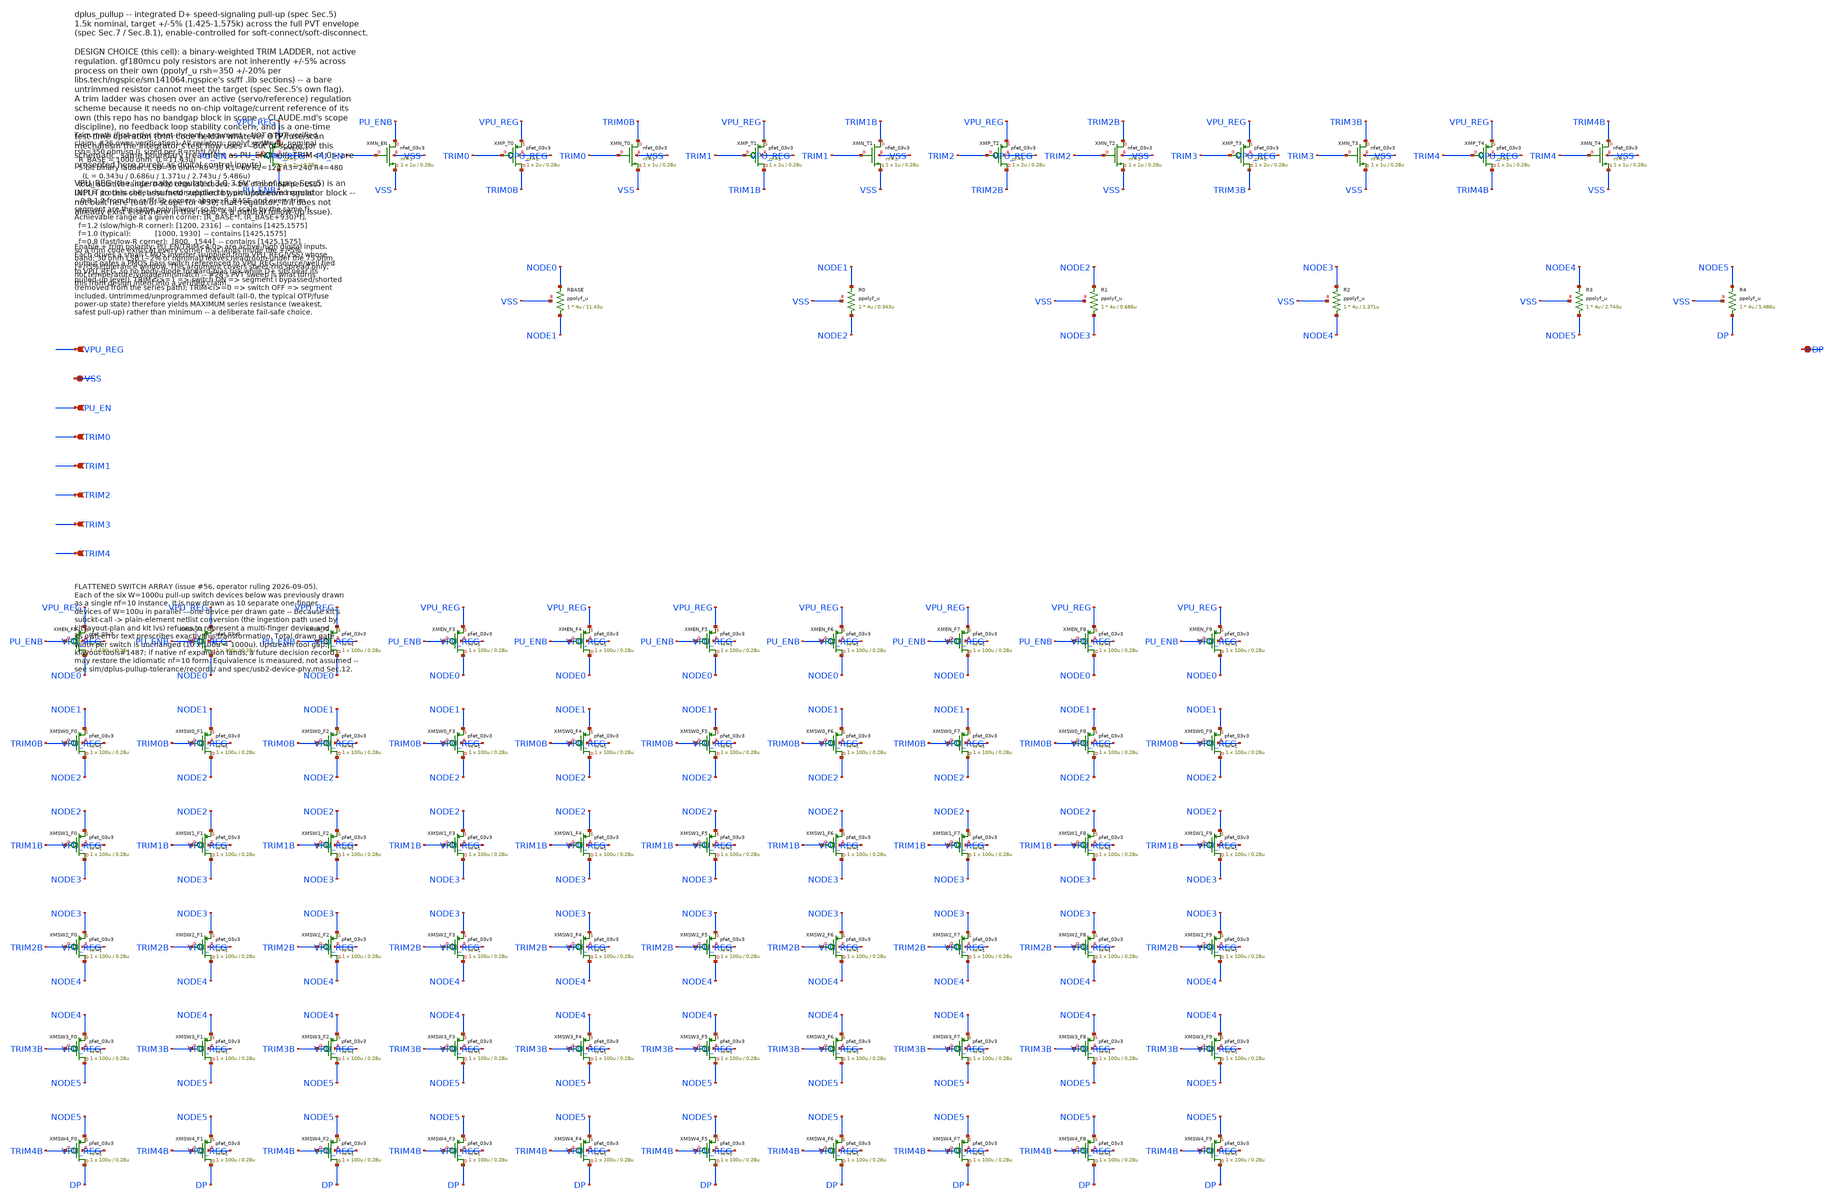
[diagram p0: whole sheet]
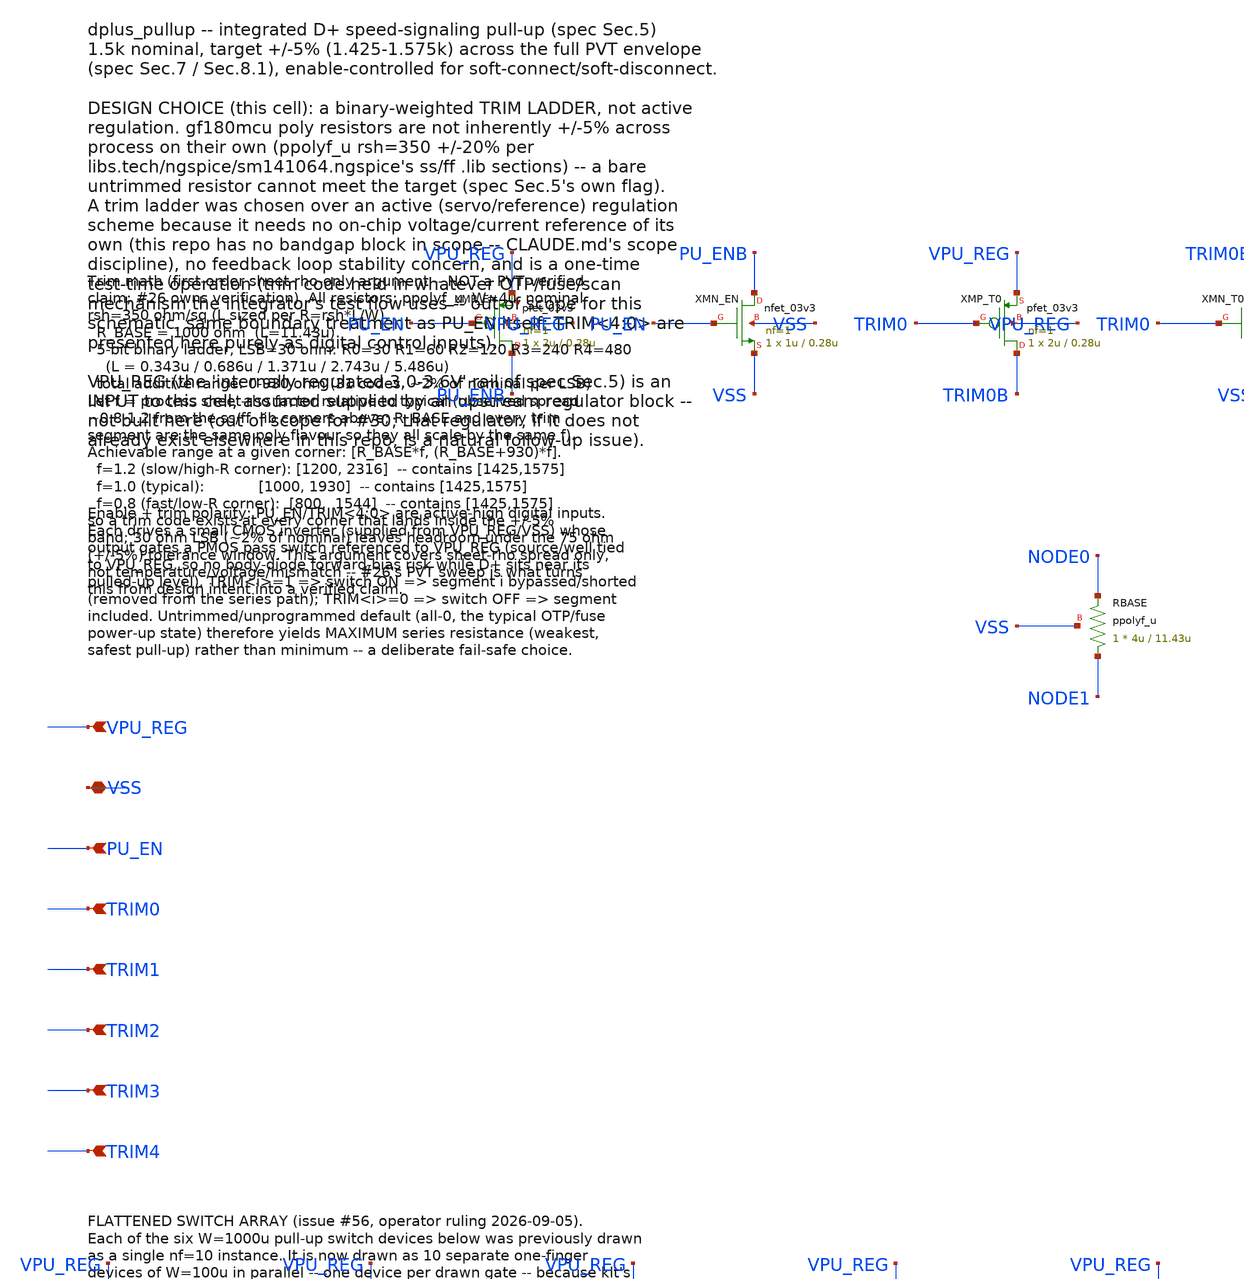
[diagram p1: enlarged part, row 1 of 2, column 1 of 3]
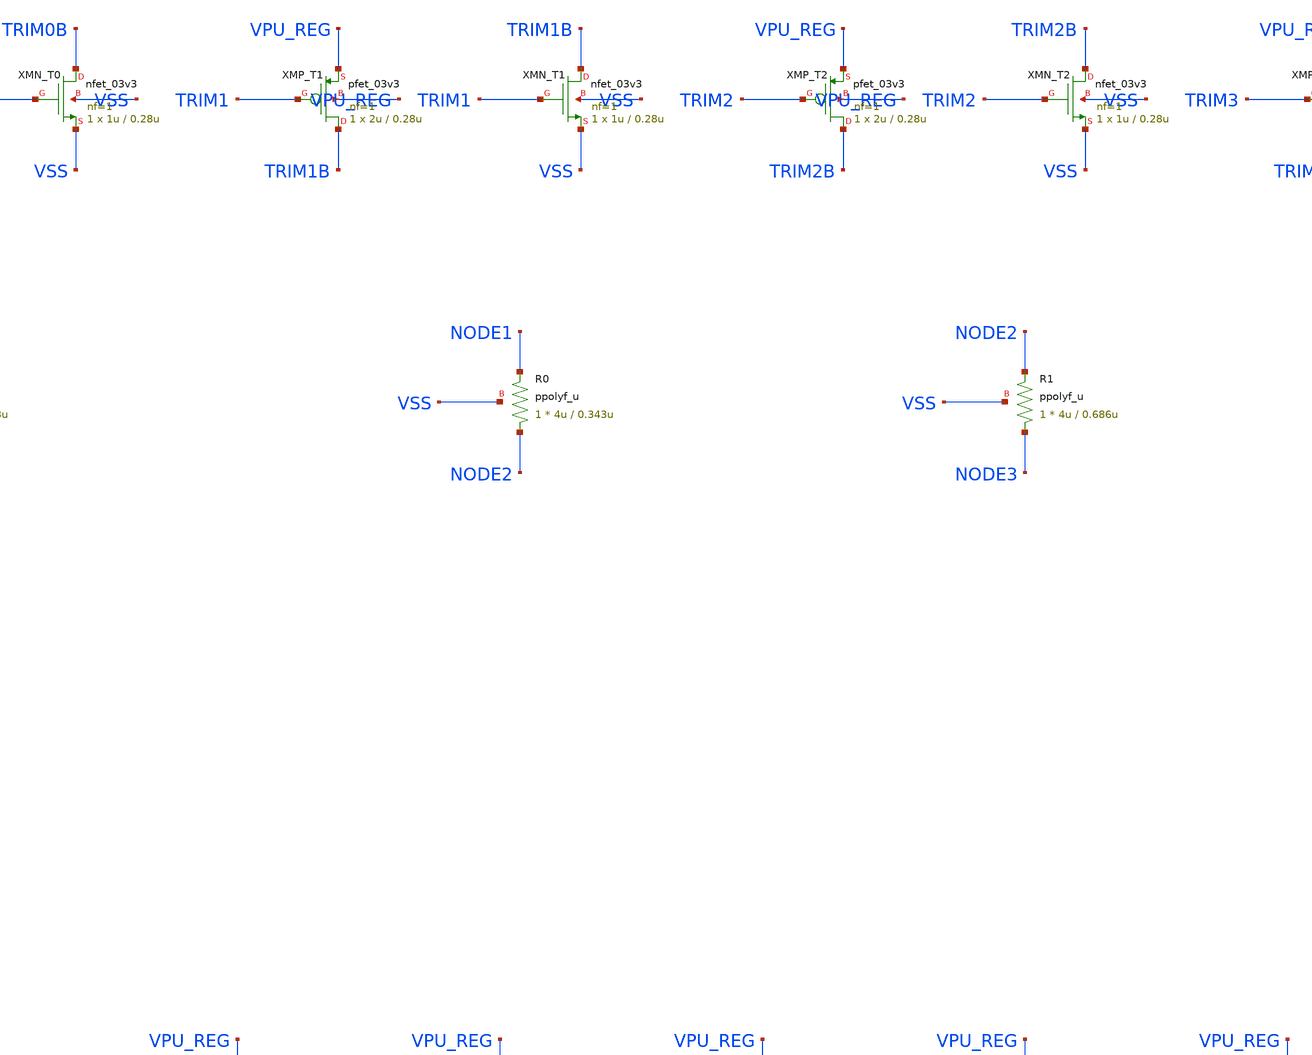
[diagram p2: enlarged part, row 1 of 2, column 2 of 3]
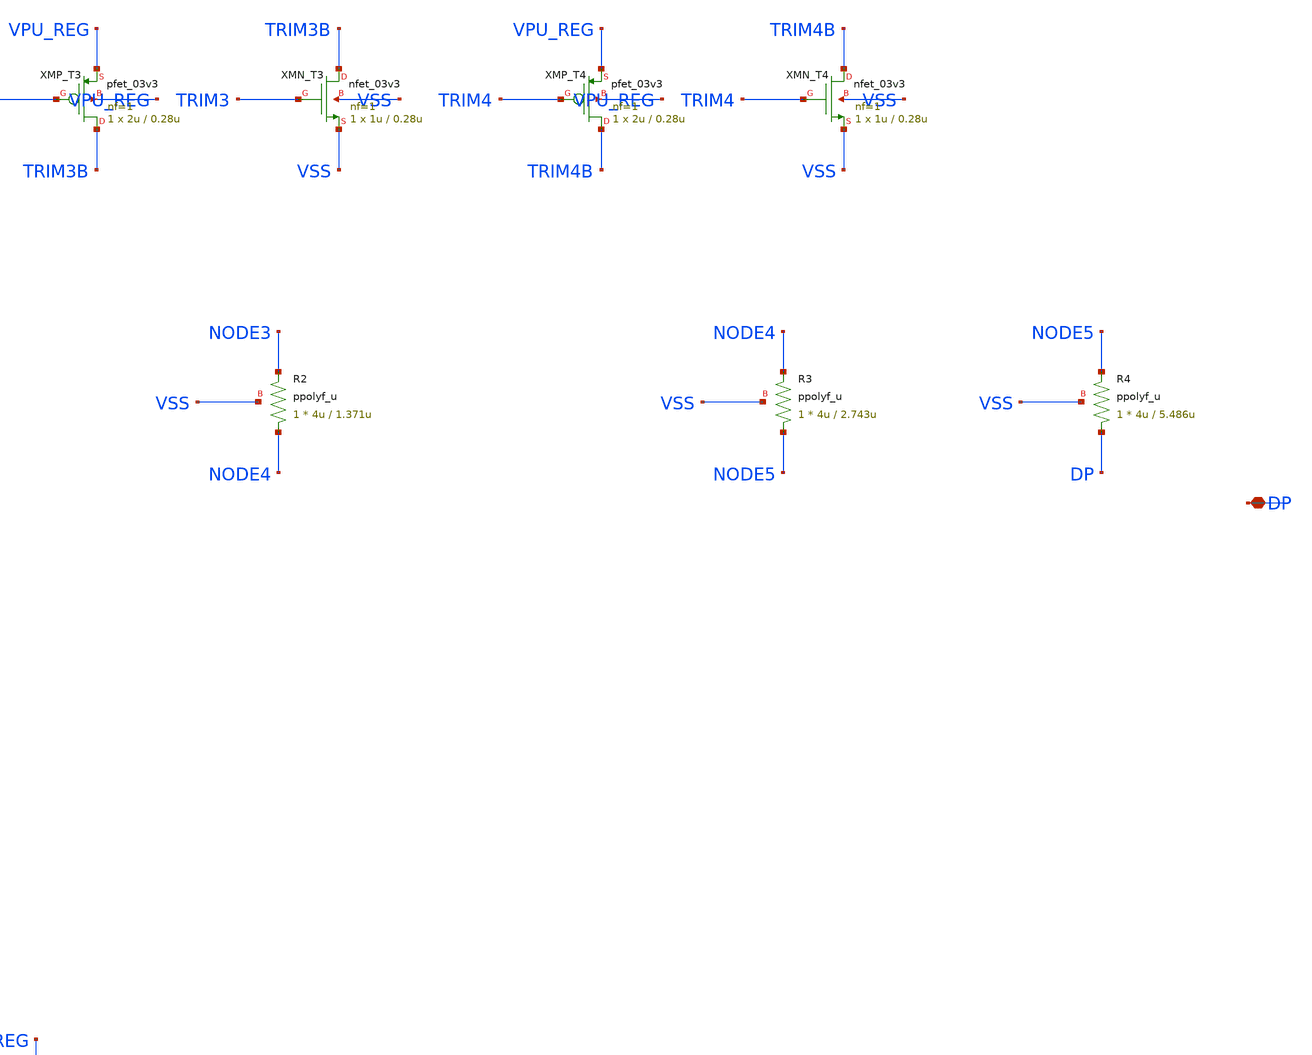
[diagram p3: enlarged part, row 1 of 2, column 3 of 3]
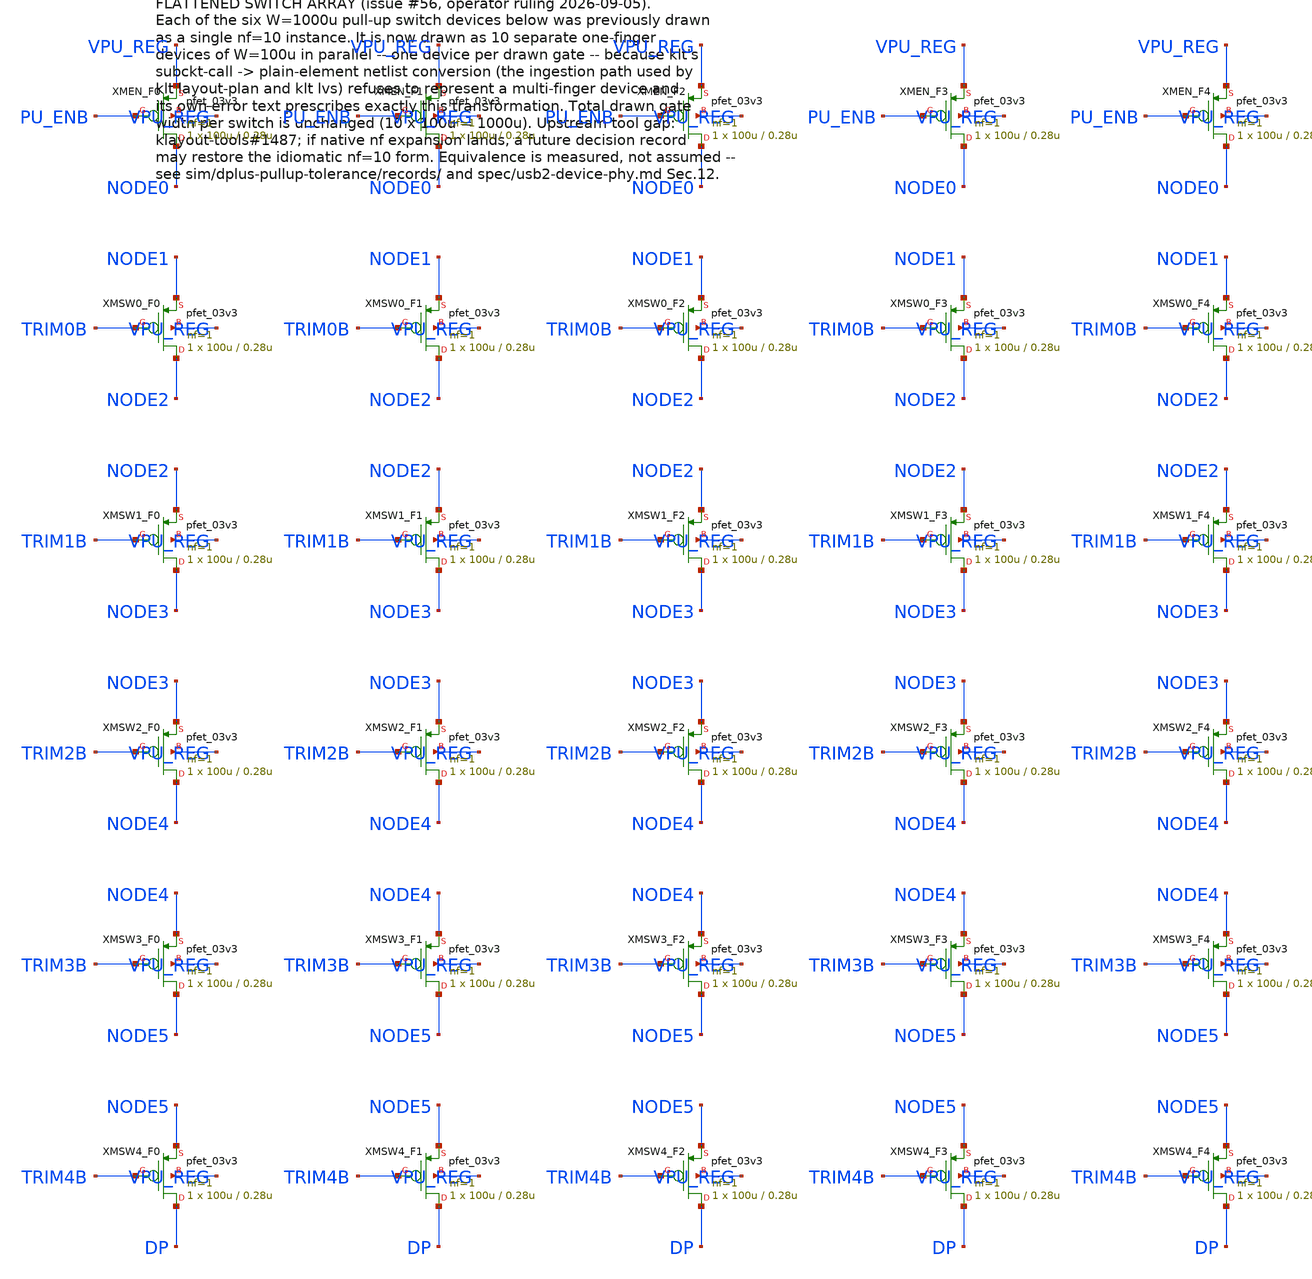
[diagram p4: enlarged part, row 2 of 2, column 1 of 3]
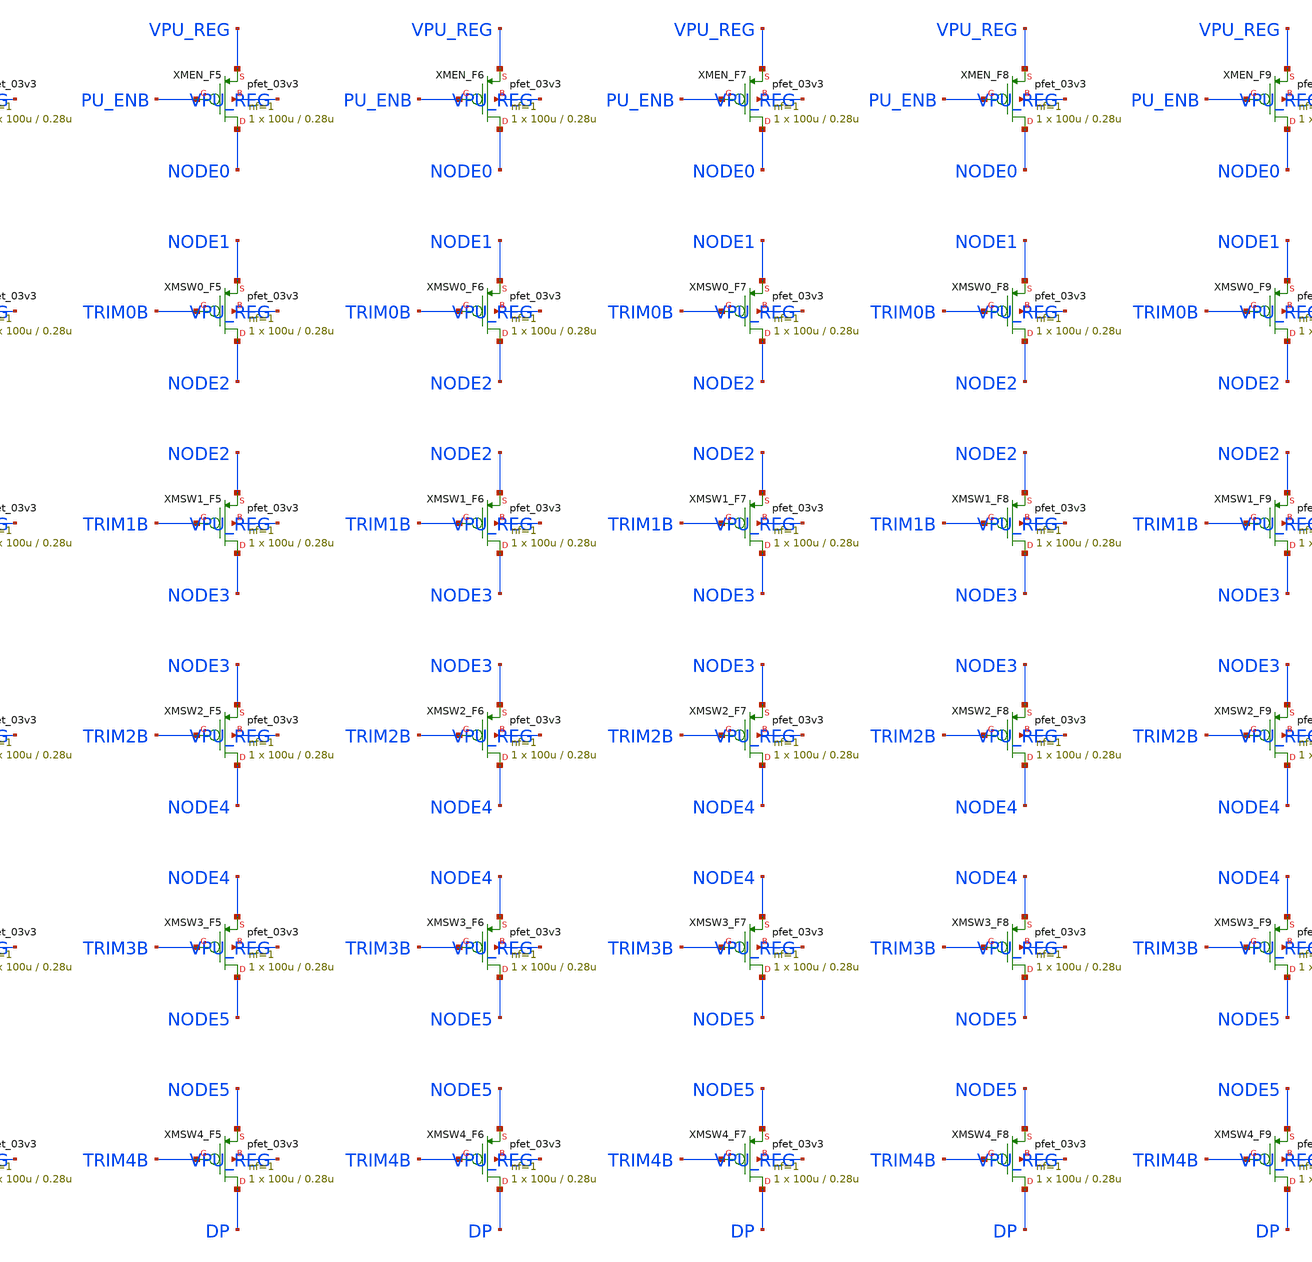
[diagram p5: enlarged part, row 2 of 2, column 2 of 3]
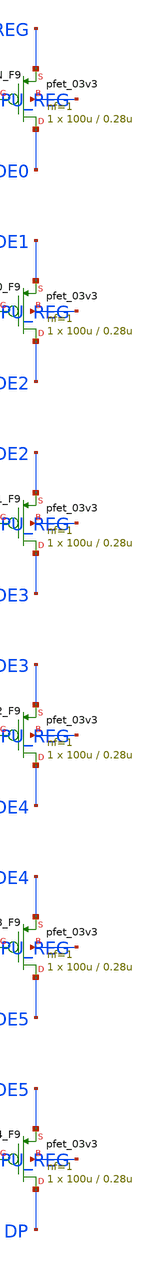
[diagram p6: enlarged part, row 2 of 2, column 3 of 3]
** sch_path: design/dplus_pullup.sch
**.subckt dplus_pullup DP VPU_REG VSS PU_EN TRIM0 TRIM1 TRIM2 TRIM3 TRIM4
*.iopin DP
*.ipin VPU_REG
*.iopin VSS
*.ipin PU_EN
*.ipin TRIM0
*.ipin TRIM1
*.ipin TRIM2
*.ipin TRIM3
*.ipin TRIM4
XMP_EN PU_ENB PU_EN VPU_REG VPU_REG pfet_03v3 L=0.28u W=2u nf=1 ad='int((nf+1)/2) * W/nf * 0.18u' as='int((nf+2)/2) * W/nf * 0.18u'
+ pd='2*int((nf+1)/2) * (W/nf + 0.18u)' ps='2*int((nf+2)/2) * (W/nf + 0.18u)' nrd='0.18u / W' nrs='0.18u / W'
+ sa=0 sb=0 sd=0 m=1
XMN_EN PU_ENB PU_EN VSS VSS nfet_03v3 L=0.28u W=1u nf=1 ad='int((nf+1)/2) * W/nf * 0.18u' as='int((nf+2)/2) * W/nf * 0.18u'
+ pd='2*int((nf+1)/2) * (W/nf + 0.18u)' ps='2*int((nf+2)/2) * (W/nf + 0.18u)' nrd='0.18u / W' nrs='0.18u / W'
+ sa=0 sb=0 sd=0 m=1
XMP_T0 TRIM0B TRIM0 VPU_REG VPU_REG pfet_03v3 L=0.28u W=2u nf=1 ad='int((nf+1)/2) * W/nf * 0.18u' as='int((nf+2)/2) * W/nf * 0.18u'
+ pd='2*int((nf+1)/2) * (W/nf + 0.18u)' ps='2*int((nf+2)/2) * (W/nf + 0.18u)' nrd='0.18u / W' nrs='0.18u / W'
+ sa=0 sb=0 sd=0 m=1
XMN_T0 TRIM0B TRIM0 VSS VSS nfet_03v3 L=0.28u W=1u nf=1 ad='int((nf+1)/2) * W/nf * 0.18u' as='int((nf+2)/2) * W/nf * 0.18u'
+ pd='2*int((nf+1)/2) * (W/nf + 0.18u)' ps='2*int((nf+2)/2) * (W/nf + 0.18u)' nrd='0.18u / W' nrs='0.18u / W'
+ sa=0 sb=0 sd=0 m=1
XMP_T1 TRIM1B TRIM1 VPU_REG VPU_REG pfet_03v3 L=0.28u W=2u nf=1 ad='int((nf+1)/2) * W/nf * 0.18u' as='int((nf+2)/2) * W/nf * 0.18u'
+ pd='2*int((nf+1)/2) * (W/nf + 0.18u)' ps='2*int((nf+2)/2) * (W/nf + 0.18u)' nrd='0.18u / W' nrs='0.18u / W'
+ sa=0 sb=0 sd=0 m=1
XMN_T1 TRIM1B TRIM1 VSS VSS nfet_03v3 L=0.28u W=1u nf=1 ad='int((nf+1)/2) * W/nf * 0.18u' as='int((nf+2)/2) * W/nf * 0.18u'
+ pd='2*int((nf+1)/2) * (W/nf + 0.18u)' ps='2*int((nf+2)/2) * (W/nf + 0.18u)' nrd='0.18u / W' nrs='0.18u / W'
+ sa=0 sb=0 sd=0 m=1
XMP_T2 TRIM2B TRIM2 VPU_REG VPU_REG pfet_03v3 L=0.28u W=2u nf=1 ad='int((nf+1)/2) * W/nf * 0.18u' as='int((nf+2)/2) * W/nf * 0.18u'
+ pd='2*int((nf+1)/2) * (W/nf + 0.18u)' ps='2*int((nf+2)/2) * (W/nf + 0.18u)' nrd='0.18u / W' nrs='0.18u / W'
+ sa=0 sb=0 sd=0 m=1
XMN_T2 TRIM2B TRIM2 VSS VSS nfet_03v3 L=0.28u W=1u nf=1 ad='int((nf+1)/2) * W/nf * 0.18u' as='int((nf+2)/2) * W/nf * 0.18u'
+ pd='2*int((nf+1)/2) * (W/nf + 0.18u)' ps='2*int((nf+2)/2) * (W/nf + 0.18u)' nrd='0.18u / W' nrs='0.18u / W'
+ sa=0 sb=0 sd=0 m=1
XMP_T3 TRIM3B TRIM3 VPU_REG VPU_REG pfet_03v3 L=0.28u W=2u nf=1 ad='int((nf+1)/2) * W/nf * 0.18u' as='int((nf+2)/2) * W/nf * 0.18u'
+ pd='2*int((nf+1)/2) * (W/nf + 0.18u)' ps='2*int((nf+2)/2) * (W/nf + 0.18u)' nrd='0.18u / W' nrs='0.18u / W'
+ sa=0 sb=0 sd=0 m=1
XMN_T3 TRIM3B TRIM3 VSS VSS nfet_03v3 L=0.28u W=1u nf=1 ad='int((nf+1)/2) * W/nf * 0.18u' as='int((nf+2)/2) * W/nf * 0.18u'
+ pd='2*int((nf+1)/2) * (W/nf + 0.18u)' ps='2*int((nf+2)/2) * (W/nf + 0.18u)' nrd='0.18u / W' nrs='0.18u / W'
+ sa=0 sb=0 sd=0 m=1
XMP_T4 TRIM4B TRIM4 VPU_REG VPU_REG pfet_03v3 L=0.28u W=2u nf=1 ad='int((nf+1)/2) * W/nf * 0.18u' as='int((nf+2)/2) * W/nf * 0.18u'
+ pd='2*int((nf+1)/2) * (W/nf + 0.18u)' ps='2*int((nf+2)/2) * (W/nf + 0.18u)' nrd='0.18u / W' nrs='0.18u / W'
+ sa=0 sb=0 sd=0 m=1
XMN_T4 TRIM4B TRIM4 VSS VSS nfet_03v3 L=0.28u W=1u nf=1 ad='int((nf+1)/2) * W/nf * 0.18u' as='int((nf+2)/2) * W/nf * 0.18u'
+ pd='2*int((nf+1)/2) * (W/nf + 0.18u)' ps='2*int((nf+2)/2) * (W/nf + 0.18u)' nrd='0.18u / W' nrs='0.18u / W'
+ sa=0 sb=0 sd=0 m=1
XRBASE NODE1 NODE0 VSS ppolyf_u r_width=4u r_length=11.43u m=1
XR0 NODE2 NODE1 VSS ppolyf_u r_width=4u r_length=0.343u m=1
XR1 NODE3 NODE2 VSS ppolyf_u r_width=4u r_length=0.686u m=1
XR2 NODE4 NODE3 VSS ppolyf_u r_width=4u r_length=1.371u m=1
XR3 NODE5 NODE4 VSS ppolyf_u r_width=4u r_length=2.743u m=1
XR4 DP NODE5 VSS ppolyf_u r_width=4u r_length=5.486u m=1
XMEN_F0 NODE0 PU_ENB VPU_REG VPU_REG pfet_03v3 L=0.28u W=100u nf=1 ad='int((nf+1)/2) * W/nf * 0.18u'
+ as='int((nf+2)/2) * W/nf * 0.18u' pd='2*int((nf+1)/2) * (W/nf + 0.18u)' ps='2*int((nf+2)/2) * (W/nf + 0.18u)'
+ nrd='0.18u / W' nrs='0.18u / W' sa=0 sb=0 sd=0 m=1
XMEN_F1 NODE0 PU_ENB VPU_REG VPU_REG pfet_03v3 L=0.28u W=100u nf=1 ad='int((nf+1)/2) * W/nf * 0.18u'
+ as='int((nf+2)/2) * W/nf * 0.18u' pd='2*int((nf+1)/2) * (W/nf + 0.18u)' ps='2*int((nf+2)/2) * (W/nf + 0.18u)'
+ nrd='0.18u / W' nrs='0.18u / W' sa=0 sb=0 sd=0 m=1
XMEN_F2 NODE0 PU_ENB VPU_REG VPU_REG pfet_03v3 L=0.28u W=100u nf=1 ad='int((nf+1)/2) * W/nf * 0.18u'
+ as='int((nf+2)/2) * W/nf * 0.18u' pd='2*int((nf+1)/2) * (W/nf + 0.18u)' ps='2*int((nf+2)/2) * (W/nf + 0.18u)'
+ nrd='0.18u / W' nrs='0.18u / W' sa=0 sb=0 sd=0 m=1
XMEN_F3 NODE0 PU_ENB VPU_REG VPU_REG pfet_03v3 L=0.28u W=100u nf=1 ad='int((nf+1)/2) * W/nf * 0.18u'
+ as='int((nf+2)/2) * W/nf * 0.18u' pd='2*int((nf+1)/2) * (W/nf + 0.18u)' ps='2*int((nf+2)/2) * (W/nf + 0.18u)'
+ nrd='0.18u / W' nrs='0.18u / W' sa=0 sb=0 sd=0 m=1
XMEN_F4 NODE0 PU_ENB VPU_REG VPU_REG pfet_03v3 L=0.28u W=100u nf=1 ad='int((nf+1)/2) * W/nf * 0.18u'
+ as='int((nf+2)/2) * W/nf * 0.18u' pd='2*int((nf+1)/2) * (W/nf + 0.18u)' ps='2*int((nf+2)/2) * (W/nf + 0.18u)'
+ nrd='0.18u / W' nrs='0.18u / W' sa=0 sb=0 sd=0 m=1
XMEN_F5 NODE0 PU_ENB VPU_REG VPU_REG pfet_03v3 L=0.28u W=100u nf=1 ad='int((nf+1)/2) * W/nf * 0.18u'
+ as='int((nf+2)/2) * W/nf * 0.18u' pd='2*int((nf+1)/2) * (W/nf + 0.18u)' ps='2*int((nf+2)/2) * (W/nf + 0.18u)'
+ nrd='0.18u / W' nrs='0.18u / W' sa=0 sb=0 sd=0 m=1
XMEN_F6 NODE0 PU_ENB VPU_REG VPU_REG pfet_03v3 L=0.28u W=100u nf=1 ad='int((nf+1)/2) * W/nf * 0.18u'
+ as='int((nf+2)/2) * W/nf * 0.18u' pd='2*int((nf+1)/2) * (W/nf + 0.18u)' ps='2*int((nf+2)/2) * (W/nf + 0.18u)'
+ nrd='0.18u / W' nrs='0.18u / W' sa=0 sb=0 sd=0 m=1
XMEN_F7 NODE0 PU_ENB VPU_REG VPU_REG pfet_03v3 L=0.28u W=100u nf=1 ad='int((nf+1)/2) * W/nf * 0.18u'
+ as='int((nf+2)/2) * W/nf * 0.18u' pd='2*int((nf+1)/2) * (W/nf + 0.18u)' ps='2*int((nf+2)/2) * (W/nf + 0.18u)'
+ nrd='0.18u / W' nrs='0.18u / W' sa=0 sb=0 sd=0 m=1
XMEN_F8 NODE0 PU_ENB VPU_REG VPU_REG pfet_03v3 L=0.28u W=100u nf=1 ad='int((nf+1)/2) * W/nf * 0.18u'
+ as='int((nf+2)/2) * W/nf * 0.18u' pd='2*int((nf+1)/2) * (W/nf + 0.18u)' ps='2*int((nf+2)/2) * (W/nf + 0.18u)'
+ nrd='0.18u / W' nrs='0.18u / W' sa=0 sb=0 sd=0 m=1
XMEN_F9 NODE0 PU_ENB VPU_REG VPU_REG pfet_03v3 L=0.28u W=100u nf=1 ad='int((nf+1)/2) * W/nf * 0.18u'
+ as='int((nf+2)/2) * W/nf * 0.18u' pd='2*int((nf+1)/2) * (W/nf + 0.18u)' ps='2*int((nf+2)/2) * (W/nf + 0.18u)'
+ nrd='0.18u / W' nrs='0.18u / W' sa=0 sb=0 sd=0 m=1
XMSW0_F0 NODE2 TRIM0B NODE1 VPU_REG pfet_03v3 L=0.28u W=100u nf=1 ad='int((nf+1)/2) * W/nf * 0.18u' as='int((nf+2)/2) * W/nf * 0.18u'
+ pd='2*int((nf+1)/2) * (W/nf + 0.18u)' ps='2*int((nf+2)/2) * (W/nf + 0.18u)' nrd='0.18u / W' nrs='0.18u / W'
+ sa=0 sb=0 sd=0 m=1
XMSW0_F1 NODE2 TRIM0B NODE1 VPU_REG pfet_03v3 L=0.28u W=100u nf=1 ad='int((nf+1)/2) * W/nf * 0.18u' as='int((nf+2)/2) * W/nf * 0.18u'
+ pd='2*int((nf+1)/2) * (W/nf + 0.18u)' ps='2*int((nf+2)/2) * (W/nf + 0.18u)' nrd='0.18u / W' nrs='0.18u / W'
+ sa=0 sb=0 sd=0 m=1
XMSW0_F2 NODE2 TRIM0B NODE1 VPU_REG pfet_03v3 L=0.28u W=100u nf=1 ad='int((nf+1)/2) * W/nf * 0.18u' as='int((nf+2)/2) * W/nf * 0.18u'
+ pd='2*int((nf+1)/2) * (W/nf + 0.18u)' ps='2*int((nf+2)/2) * (W/nf + 0.18u)' nrd='0.18u / W' nrs='0.18u / W'
+ sa=0 sb=0 sd=0 m=1
XMSW0_F3 NODE2 TRIM0B NODE1 VPU_REG pfet_03v3 L=0.28u W=100u nf=1 ad='int((nf+1)/2) * W/nf * 0.18u' as='int((nf+2)/2) * W/nf * 0.18u'
+ pd='2*int((nf+1)/2) * (W/nf + 0.18u)' ps='2*int((nf+2)/2) * (W/nf + 0.18u)' nrd='0.18u / W' nrs='0.18u / W'
+ sa=0 sb=0 sd=0 m=1
XMSW0_F4 NODE2 TRIM0B NODE1 VPU_REG pfet_03v3 L=0.28u W=100u nf=1 ad='int((nf+1)/2) * W/nf * 0.18u' as='int((nf+2)/2) * W/nf * 0.18u'
+ pd='2*int((nf+1)/2) * (W/nf + 0.18u)' ps='2*int((nf+2)/2) * (W/nf + 0.18u)' nrd='0.18u / W' nrs='0.18u / W'
+ sa=0 sb=0 sd=0 m=1
XMSW0_F5 NODE2 TRIM0B NODE1 VPU_REG pfet_03v3 L=0.28u W=100u nf=1 ad='int((nf+1)/2) * W/nf * 0.18u' as='int((nf+2)/2) * W/nf * 0.18u'
+ pd='2*int((nf+1)/2) * (W/nf + 0.18u)' ps='2*int((nf+2)/2) * (W/nf + 0.18u)' nrd='0.18u / W' nrs='0.18u / W'
+ sa=0 sb=0 sd=0 m=1
XMSW0_F6 NODE2 TRIM0B NODE1 VPU_REG pfet_03v3 L=0.28u W=100u nf=1 ad='int((nf+1)/2) * W/nf * 0.18u' as='int((nf+2)/2) * W/nf * 0.18u'
+ pd='2*int((nf+1)/2) * (W/nf + 0.18u)' ps='2*int((nf+2)/2) * (W/nf + 0.18u)' nrd='0.18u / W' nrs='0.18u / W'
+ sa=0 sb=0 sd=0 m=1
XMSW0_F7 NODE2 TRIM0B NODE1 VPU_REG pfet_03v3 L=0.28u W=100u nf=1 ad='int((nf+1)/2) * W/nf * 0.18u' as='int((nf+2)/2) * W/nf * 0.18u'
+ pd='2*int((nf+1)/2) * (W/nf + 0.18u)' ps='2*int((nf+2)/2) * (W/nf + 0.18u)' nrd='0.18u / W' nrs='0.18u / W'
+ sa=0 sb=0 sd=0 m=1
XMSW0_F8 NODE2 TRIM0B NODE1 VPU_REG pfet_03v3 L=0.28u W=100u nf=1 ad='int((nf+1)/2) * W/nf * 0.18u' as='int((nf+2)/2) * W/nf * 0.18u'
+ pd='2*int((nf+1)/2) * (W/nf + 0.18u)' ps='2*int((nf+2)/2) * (W/nf + 0.18u)' nrd='0.18u / W' nrs='0.18u / W'
+ sa=0 sb=0 sd=0 m=1
XMSW0_F9 NODE2 TRIM0B NODE1 VPU_REG pfet_03v3 L=0.28u W=100u nf=1 ad='int((nf+1)/2) * W/nf * 0.18u' as='int((nf+2)/2) * W/nf * 0.18u'
+ pd='2*int((nf+1)/2) * (W/nf + 0.18u)' ps='2*int((nf+2)/2) * (W/nf + 0.18u)' nrd='0.18u / W' nrs='0.18u / W'
+ sa=0 sb=0 sd=0 m=1
XMSW1_F0 NODE3 TRIM1B NODE2 VPU_REG pfet_03v3 L=0.28u W=100u nf=1 ad='int((nf+1)/2) * W/nf * 0.18u' as='int((nf+2)/2) * W/nf * 0.18u'
+ pd='2*int((nf+1)/2) * (W/nf + 0.18u)' ps='2*int((nf+2)/2) * (W/nf + 0.18u)' nrd='0.18u / W' nrs='0.18u / W'
+ sa=0 sb=0 sd=0 m=1
XMSW1_F1 NODE3 TRIM1B NODE2 VPU_REG pfet_03v3 L=0.28u W=100u nf=1 ad='int((nf+1)/2) * W/nf * 0.18u' as='int((nf+2)/2) * W/nf * 0.18u'
+ pd='2*int((nf+1)/2) * (W/nf + 0.18u)' ps='2*int((nf+2)/2) * (W/nf + 0.18u)' nrd='0.18u / W' nrs='0.18u / W'
+ sa=0 sb=0 sd=0 m=1
XMSW1_F2 NODE3 TRIM1B NODE2 VPU_REG pfet_03v3 L=0.28u W=100u nf=1 ad='int((nf+1)/2) * W/nf * 0.18u' as='int((nf+2)/2) * W/nf * 0.18u'
+ pd='2*int((nf+1)/2) * (W/nf + 0.18u)' ps='2*int((nf+2)/2) * (W/nf + 0.18u)' nrd='0.18u / W' nrs='0.18u / W'
+ sa=0 sb=0 sd=0 m=1
XMSW1_F3 NODE3 TRIM1B NODE2 VPU_REG pfet_03v3 L=0.28u W=100u nf=1 ad='int((nf+1)/2) * W/nf * 0.18u' as='int((nf+2)/2) * W/nf * 0.18u'
+ pd='2*int((nf+1)/2) * (W/nf + 0.18u)' ps='2*int((nf+2)/2) * (W/nf + 0.18u)' nrd='0.18u / W' nrs='0.18u / W'
+ sa=0 sb=0 sd=0 m=1
XMSW1_F4 NODE3 TRIM1B NODE2 VPU_REG pfet_03v3 L=0.28u W=100u nf=1 ad='int((nf+1)/2) * W/nf * 0.18u' as='int((nf+2)/2) * W/nf * 0.18u'
+ pd='2*int((nf+1)/2) * (W/nf + 0.18u)' ps='2*int((nf+2)/2) * (W/nf + 0.18u)' nrd='0.18u / W' nrs='0.18u / W'
+ sa=0 sb=0 sd=0 m=1
XMSW1_F5 NODE3 TRIM1B NODE2 VPU_REG pfet_03v3 L=0.28u W=100u nf=1 ad='int((nf+1)/2) * W/nf * 0.18u' as='int((nf+2)/2) * W/nf * 0.18u'
+ pd='2*int((nf+1)/2) * (W/nf + 0.18u)' ps='2*int((nf+2)/2) * (W/nf + 0.18u)' nrd='0.18u / W' nrs='0.18u / W'
+ sa=0 sb=0 sd=0 m=1
XMSW1_F6 NODE3 TRIM1B NODE2 VPU_REG pfet_03v3 L=0.28u W=100u nf=1 ad='int((nf+1)/2) * W/nf * 0.18u' as='int((nf+2)/2) * W/nf * 0.18u'
+ pd='2*int((nf+1)/2) * (W/nf + 0.18u)' ps='2*int((nf+2)/2) * (W/nf + 0.18u)' nrd='0.18u / W' nrs='0.18u / W'
+ sa=0 sb=0 sd=0 m=1
XMSW1_F7 NODE3 TRIM1B NODE2 VPU_REG pfet_03v3 L=0.28u W=100u nf=1 ad='int((nf+1)/2) * W/nf * 0.18u' as='int((nf+2)/2) * W/nf * 0.18u'
+ pd='2*int((nf+1)/2) * (W/nf + 0.18u)' ps='2*int((nf+2)/2) * (W/nf + 0.18u)' nrd='0.18u / W' nrs='0.18u / W'
+ sa=0 sb=0 sd=0 m=1
XMSW1_F8 NODE3 TRIM1B NODE2 VPU_REG pfet_03v3 L=0.28u W=100u nf=1 ad='int((nf+1)/2) * W/nf * 0.18u' as='int((nf+2)/2) * W/nf * 0.18u'
+ pd='2*int((nf+1)/2) * (W/nf + 0.18u)' ps='2*int((nf+2)/2) * (W/nf + 0.18u)' nrd='0.18u / W' nrs='0.18u / W'
+ sa=0 sb=0 sd=0 m=1
XMSW1_F9 NODE3 TRIM1B NODE2 VPU_REG pfet_03v3 L=0.28u W=100u nf=1 ad='int((nf+1)/2) * W/nf * 0.18u' as='int((nf+2)/2) * W/nf * 0.18u'
+ pd='2*int((nf+1)/2) * (W/nf + 0.18u)' ps='2*int((nf+2)/2) * (W/nf + 0.18u)' nrd='0.18u / W' nrs='0.18u / W'
+ sa=0 sb=0 sd=0 m=1
XMSW2_F0 NODE4 TRIM2B NODE3 VPU_REG pfet_03v3 L=0.28u W=100u nf=1 ad='int((nf+1)/2) * W/nf * 0.18u' as='int((nf+2)/2) * W/nf * 0.18u'
+ pd='2*int((nf+1)/2) * (W/nf + 0.18u)' ps='2*int((nf+2)/2) * (W/nf + 0.18u)' nrd='0.18u / W' nrs='0.18u / W'
+ sa=0 sb=0 sd=0 m=1
XMSW2_F1 NODE4 TRIM2B NODE3 VPU_REG pfet_03v3 L=0.28u W=100u nf=1 ad='int((nf+1)/2) * W/nf * 0.18u' as='int((nf+2)/2) * W/nf * 0.18u'
+ pd='2*int((nf+1)/2) * (W/nf + 0.18u)' ps='2*int((nf+2)/2) * (W/nf + 0.18u)' nrd='0.18u / W' nrs='0.18u / W'
+ sa=0 sb=0 sd=0 m=1
XMSW2_F2 NODE4 TRIM2B NODE3 VPU_REG pfet_03v3 L=0.28u W=100u nf=1 ad='int((nf+1)/2) * W/nf * 0.18u' as='int((nf+2)/2) * W/nf * 0.18u'
+ pd='2*int((nf+1)/2) * (W/nf + 0.18u)' ps='2*int((nf+2)/2) * (W/nf + 0.18u)' nrd='0.18u / W' nrs='0.18u / W'
+ sa=0 sb=0 sd=0 m=1
XMSW2_F3 NODE4 TRIM2B NODE3 VPU_REG pfet_03v3 L=0.28u W=100u nf=1 ad='int((nf+1)/2) * W/nf * 0.18u' as='int((nf+2)/2) * W/nf * 0.18u'
+ pd='2*int((nf+1)/2) * (W/nf + 0.18u)' ps='2*int((nf+2)/2) * (W/nf + 0.18u)' nrd='0.18u / W' nrs='0.18u / W'
+ sa=0 sb=0 sd=0 m=1
XMSW2_F4 NODE4 TRIM2B NODE3 VPU_REG pfet_03v3 L=0.28u W=100u nf=1 ad='int((nf+1)/2) * W/nf * 0.18u' as='int((nf+2)/2) * W/nf * 0.18u'
+ pd='2*int((nf+1)/2) * (W/nf + 0.18u)' ps='2*int((nf+2)/2) * (W/nf + 0.18u)' nrd='0.18u / W' nrs='0.18u / W'
+ sa=0 sb=0 sd=0 m=1
XMSW2_F5 NODE4 TRIM2B NODE3 VPU_REG pfet_03v3 L=0.28u W=100u nf=1 ad='int((nf+1)/2) * W/nf * 0.18u' as='int((nf+2)/2) * W/nf * 0.18u'
+ pd='2*int((nf+1)/2) * (W/nf + 0.18u)' ps='2*int((nf+2)/2) * (W/nf + 0.18u)' nrd='0.18u / W' nrs='0.18u / W'
+ sa=0 sb=0 sd=0 m=1
XMSW2_F6 NODE4 TRIM2B NODE3 VPU_REG pfet_03v3 L=0.28u W=100u nf=1 ad='int((nf+1)/2) * W/nf * 0.18u' as='int((nf+2)/2) * W/nf * 0.18u'
+ pd='2*int((nf+1)/2) * (W/nf + 0.18u)' ps='2*int((nf+2)/2) * (W/nf + 0.18u)' nrd='0.18u / W' nrs='0.18u / W'
+ sa=0 sb=0 sd=0 m=1
XMSW2_F7 NODE4 TRIM2B NODE3 VPU_REG pfet_03v3 L=0.28u W=100u nf=1 ad='int((nf+1)/2) * W/nf * 0.18u' as='int((nf+2)/2) * W/nf * 0.18u'
+ pd='2*int((nf+1)/2) * (W/nf + 0.18u)' ps='2*int((nf+2)/2) * (W/nf + 0.18u)' nrd='0.18u / W' nrs='0.18u / W'
+ sa=0 sb=0 sd=0 m=1
XMSW2_F8 NODE4 TRIM2B NODE3 VPU_REG pfet_03v3 L=0.28u W=100u nf=1 ad='int((nf+1)/2) * W/nf * 0.18u' as='int((nf+2)/2) * W/nf * 0.18u'
+ pd='2*int((nf+1)/2) * (W/nf + 0.18u)' ps='2*int((nf+2)/2) * (W/nf + 0.18u)' nrd='0.18u / W' nrs='0.18u / W'
+ sa=0 sb=0 sd=0 m=1
XMSW2_F9 NODE4 TRIM2B NODE3 VPU_REG pfet_03v3 L=0.28u W=100u nf=1 ad='int((nf+1)/2) * W/nf * 0.18u' as='int((nf+2)/2) * W/nf * 0.18u'
+ pd='2*int((nf+1)/2) * (W/nf + 0.18u)' ps='2*int((nf+2)/2) * (W/nf + 0.18u)' nrd='0.18u / W' nrs='0.18u / W'
+ sa=0 sb=0 sd=0 m=1
XMSW3_F0 NODE5 TRIM3B NODE4 VPU_REG pfet_03v3 L=0.28u W=100u nf=1 ad='int((nf+1)/2) * W/nf * 0.18u' as='int((nf+2)/2) * W/nf * 0.18u'
+ pd='2*int((nf+1)/2) * (W/nf + 0.18u)' ps='2*int((nf+2)/2) * (W/nf + 0.18u)' nrd='0.18u / W' nrs='0.18u / W'
+ sa=0 sb=0 sd=0 m=1
XMSW3_F1 NODE5 TRIM3B NODE4 VPU_REG pfet_03v3 L=0.28u W=100u nf=1 ad='int((nf+1)/2) * W/nf * 0.18u' as='int((nf+2)/2) * W/nf * 0.18u'
+ pd='2*int((nf+1)/2) * (W/nf + 0.18u)' ps='2*int((nf+2)/2) * (W/nf + 0.18u)' nrd='0.18u / W' nrs='0.18u / W'
+ sa=0 sb=0 sd=0 m=1
XMSW3_F2 NODE5 TRIM3B NODE4 VPU_REG pfet_03v3 L=0.28u W=100u nf=1 ad='int((nf+1)/2) * W/nf * 0.18u' as='int((nf+2)/2) * W/nf * 0.18u'
+ pd='2*int((nf+1)/2) * (W/nf + 0.18u)' ps='2*int((nf+2)/2) * (W/nf + 0.18u)' nrd='0.18u / W' nrs='0.18u / W'
+ sa=0 sb=0 sd=0 m=1
XMSW3_F3 NODE5 TRIM3B NODE4 VPU_REG pfet_03v3 L=0.28u W=100u nf=1 ad='int((nf+1)/2) * W/nf * 0.18u' as='int((nf+2)/2) * W/nf * 0.18u'
+ pd='2*int((nf+1)/2) * (W/nf + 0.18u)' ps='2*int((nf+2)/2) * (W/nf + 0.18u)' nrd='0.18u / W' nrs='0.18u / W'
+ sa=0 sb=0 sd=0 m=1
XMSW3_F4 NODE5 TRIM3B NODE4 VPU_REG pfet_03v3 L=0.28u W=100u nf=1 ad='int((nf+1)/2) * W/nf * 0.18u' as='int((nf+2)/2) * W/nf * 0.18u'
+ pd='2*int((nf+1)/2) * (W/nf + 0.18u)' ps='2*int((nf+2)/2) * (W/nf + 0.18u)' nrd='0.18u / W' nrs='0.18u / W'
+ sa=0 sb=0 sd=0 m=1
XMSW3_F5 NODE5 TRIM3B NODE4 VPU_REG pfet_03v3 L=0.28u W=100u nf=1 ad='int((nf+1)/2) * W/nf * 0.18u' as='int((nf+2)/2) * W/nf * 0.18u'
+ pd='2*int((nf+1)/2) * (W/nf + 0.18u)' ps='2*int((nf+2)/2) * (W/nf + 0.18u)' nrd='0.18u / W' nrs='0.18u / W'
+ sa=0 sb=0 sd=0 m=1
XMSW3_F6 NODE5 TRIM3B NODE4 VPU_REG pfet_03v3 L=0.28u W=100u nf=1 ad='int((nf+1)/2) * W/nf * 0.18u' as='int((nf+2)/2) * W/nf * 0.18u'
+ pd='2*int((nf+1)/2) * (W/nf + 0.18u)' ps='2*int((nf+2)/2) * (W/nf + 0.18u)' nrd='0.18u / W' nrs='0.18u / W'
+ sa=0 sb=0 sd=0 m=1
XMSW3_F7 NODE5 TRIM3B NODE4 VPU_REG pfet_03v3 L=0.28u W=100u nf=1 ad='int((nf+1)/2) * W/nf * 0.18u' as='int((nf+2)/2) * W/nf * 0.18u'
+ pd='2*int((nf+1)/2) * (W/nf + 0.18u)' ps='2*int((nf+2)/2) * (W/nf + 0.18u)' nrd='0.18u / W' nrs='0.18u / W'
+ sa=0 sb=0 sd=0 m=1
XMSW3_F8 NODE5 TRIM3B NODE4 VPU_REG pfet_03v3 L=0.28u W=100u nf=1 ad='int((nf+1)/2) * W/nf * 0.18u' as='int((nf+2)/2) * W/nf * 0.18u'
+ pd='2*int((nf+1)/2) * (W/nf + 0.18u)' ps='2*int((nf+2)/2) * (W/nf + 0.18u)' nrd='0.18u / W' nrs='0.18u / W'
+ sa=0 sb=0 sd=0 m=1
XMSW3_F9 NODE5 TRIM3B NODE4 VPU_REG pfet_03v3 L=0.28u W=100u nf=1 ad='int((nf+1)/2) * W/nf * 0.18u' as='int((nf+2)/2) * W/nf * 0.18u'
+ pd='2*int((nf+1)/2) * (W/nf + 0.18u)' ps='2*int((nf+2)/2) * (W/nf + 0.18u)' nrd='0.18u / W' nrs='0.18u / W'
+ sa=0 sb=0 sd=0 m=1
XMSW4_F0 DP TRIM4B NODE5 VPU_REG pfet_03v3 L=0.28u W=100u nf=1 ad='int((nf+1)/2) * W/nf * 0.18u' as='int((nf+2)/2) * W/nf * 0.18u'
+ pd='2*int((nf+1)/2) * (W/nf + 0.18u)' ps='2*int((nf+2)/2) * (W/nf + 0.18u)' nrd='0.18u / W' nrs='0.18u / W'
+ sa=0 sb=0 sd=0 m=1
XMSW4_F1 DP TRIM4B NODE5 VPU_REG pfet_03v3 L=0.28u W=100u nf=1 ad='int((nf+1)/2) * W/nf * 0.18u' as='int((nf+2)/2) * W/nf * 0.18u'
+ pd='2*int((nf+1)/2) * (W/nf + 0.18u)' ps='2*int((nf+2)/2) * (W/nf + 0.18u)' nrd='0.18u / W' nrs='0.18u / W'
+ sa=0 sb=0 sd=0 m=1
XMSW4_F2 DP TRIM4B NODE5 VPU_REG pfet_03v3 L=0.28u W=100u nf=1 ad='int((nf+1)/2) * W/nf * 0.18u' as='int((nf+2)/2) * W/nf * 0.18u'
+ pd='2*int((nf+1)/2) * (W/nf + 0.18u)' ps='2*int((nf+2)/2) * (W/nf + 0.18u)' nrd='0.18u / W' nrs='0.18u / W'
+ sa=0 sb=0 sd=0 m=1
XMSW4_F3 DP TRIM4B NODE5 VPU_REG pfet_03v3 L=0.28u W=100u nf=1 ad='int((nf+1)/2) * W/nf * 0.18u' as='int((nf+2)/2) * W/nf * 0.18u'
+ pd='2*int((nf+1)/2) * (W/nf + 0.18u)' ps='2*int((nf+2)/2) * (W/nf + 0.18u)' nrd='0.18u / W' nrs='0.18u / W'
+ sa=0 sb=0 sd=0 m=1
XMSW4_F4 DP TRIM4B NODE5 VPU_REG pfet_03v3 L=0.28u W=100u nf=1 ad='int((nf+1)/2) * W/nf * 0.18u' as='int((nf+2)/2) * W/nf * 0.18u'
+ pd='2*int((nf+1)/2) * (W/nf + 0.18u)' ps='2*int((nf+2)/2) * (W/nf + 0.18u)' nrd='0.18u / W' nrs='0.18u / W'
+ sa=0 sb=0 sd=0 m=1
XMSW4_F5 DP TRIM4B NODE5 VPU_REG pfet_03v3 L=0.28u W=100u nf=1 ad='int((nf+1)/2) * W/nf * 0.18u' as='int((nf+2)/2) * W/nf * 0.18u'
+ pd='2*int((nf+1)/2) * (W/nf + 0.18u)' ps='2*int((nf+2)/2) * (W/nf + 0.18u)' nrd='0.18u / W' nrs='0.18u / W'
+ sa=0 sb=0 sd=0 m=1
XMSW4_F6 DP TRIM4B NODE5 VPU_REG pfet_03v3 L=0.28u W=100u nf=1 ad='int((nf+1)/2) * W/nf * 0.18u' as='int((nf+2)/2) * W/nf * 0.18u'
+ pd='2*int((nf+1)/2) * (W/nf + 0.18u)' ps='2*int((nf+2)/2) * (W/nf + 0.18u)' nrd='0.18u / W' nrs='0.18u / W'
+ sa=0 sb=0 sd=0 m=1
XMSW4_F7 DP TRIM4B NODE5 VPU_REG pfet_03v3 L=0.28u W=100u nf=1 ad='int((nf+1)/2) * W/nf * 0.18u' as='int((nf+2)/2) * W/nf * 0.18u'
+ pd='2*int((nf+1)/2) * (W/nf + 0.18u)' ps='2*int((nf+2)/2) * (W/nf + 0.18u)' nrd='0.18u / W' nrs='0.18u / W'
+ sa=0 sb=0 sd=0 m=1
XMSW4_F8 DP TRIM4B NODE5 VPU_REG pfet_03v3 L=0.28u W=100u nf=1 ad='int((nf+1)/2) * W/nf * 0.18u' as='int((nf+2)/2) * W/nf * 0.18u'
+ pd='2*int((nf+1)/2) * (W/nf + 0.18u)' ps='2*int((nf+2)/2) * (W/nf + 0.18u)' nrd='0.18u / W' nrs='0.18u / W'
+ sa=0 sb=0 sd=0 m=1
XMSW4_F9 DP TRIM4B NODE5 VPU_REG pfet_03v3 L=0.28u W=100u nf=1 ad='int((nf+1)/2) * W/nf * 0.18u' as='int((nf+2)/2) * W/nf * 0.18u'
+ pd='2*int((nf+1)/2) * (W/nf + 0.18u)' ps='2*int((nf+2)/2) * (W/nf + 0.18u)' nrd='0.18u / W' nrs='0.18u / W'
+ sa=0 sb=0 sd=0 m=1
**.ends
.end
